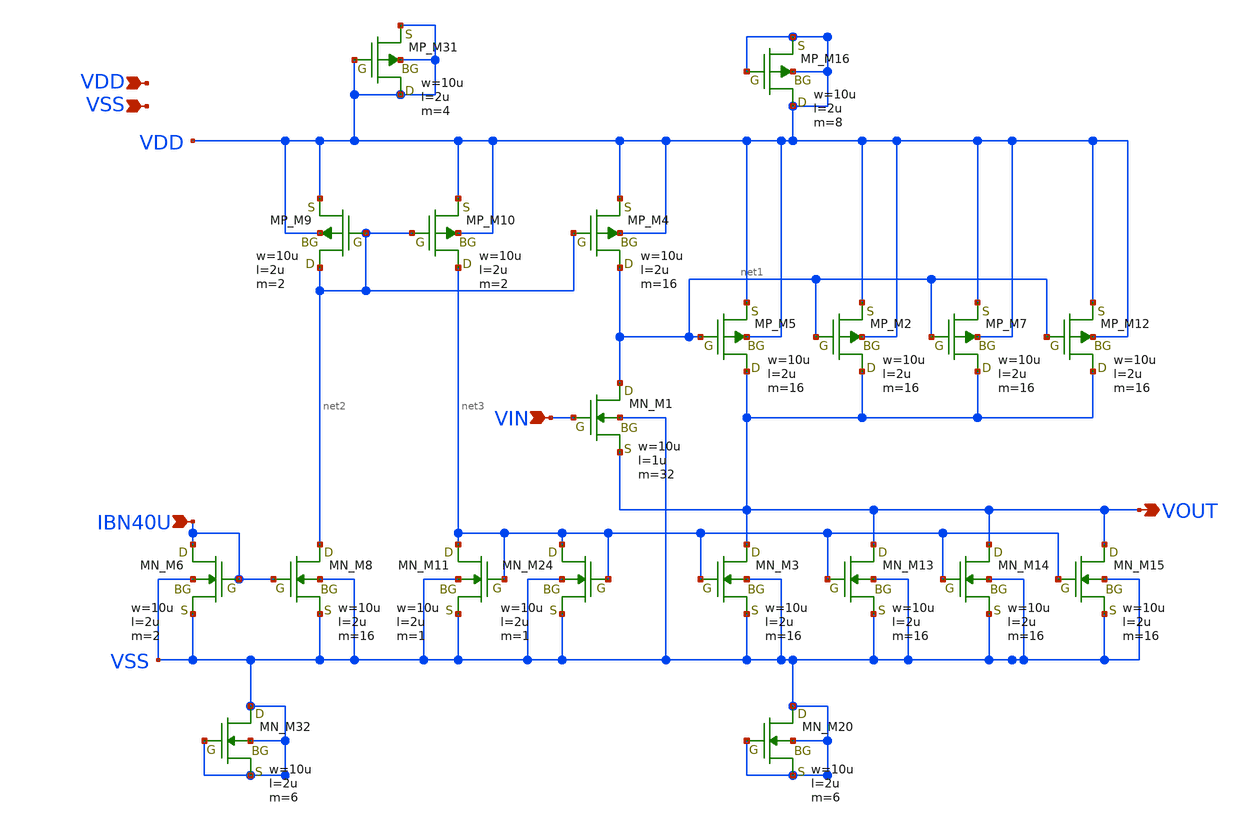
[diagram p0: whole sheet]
** sch_path: member_project/JJY_Receiver/Masahiro/jjy_recv/OBUF_SSF/BUF_SSF.sch
**.subckt BUF_SSF VDD VSS VIN IBN40U VOUT
*.ipin VDD
*.ipin VSS
*.ipin VIN
*.ipin IBN40U
*.opin VOUT
XM1 net1 VIN VOUT VSS NMOS w=10u l=1u as=0 ad=0 ps=0 pd=0 nrd=0 nrs=0 m=32
XM3 VOUT net3 VSS VSS NMOS w=10u l=2u as=0 ad=0 ps=0 pd=0 nrd=0 nrs=0 m=16
XM6 IBN40U IBN40U VSS VSS NMOS w=10u l=2u as=0 ad=0 ps=0 pd=0 nrd=0 nrs=0 m=2
XM4 net1 net2 VDD VDD PMOS w=10u l=2u as=0 ad=0 ps=0 pd=0 nrd=0 nrs=0 m=16
XM5 VOUT net1 VDD VDD PMOS w=10u l=2u as=0 ad=0 ps=0 pd=0 nrd=0 nrs=0 m=16
XM8 net2 IBN40U VSS VSS NMOS w=10u l=2u as=0 ad=0 ps=0 pd=0 nrd=0 nrs=0 m=16
XM9 net2 net2 VDD VDD PMOS w=10u l=2u as=0 ad=0 ps=0 pd=0 nrd=0 nrs=0 m=2
XM10 net3 net2 VDD VDD PMOS w=10u l=2u as=0 ad=0 ps=0 pd=0 nrd=0 nrs=0 m=2
XM11 net3 net3 VSS VSS NMOS w=10u l=2u as=0 ad=0 ps=0 pd=0 nrd=0 nrs=0 m=1
XM2 VOUT net1 VDD VDD PMOS w=10u l=2u as=0 ad=0 ps=0 pd=0 nrd=0 nrs=0 m=16
XM7 VOUT net1 VDD VDD PMOS w=10u l=2u as=0 ad=0 ps=0 pd=0 nrd=0 nrs=0 m=16
XM12 VOUT net1 VDD VDD PMOS w=10u l=2u as=0 ad=0 ps=0 pd=0 nrd=0 nrs=0 m=16
XM13 VOUT net3 VSS VSS NMOS w=10u l=2u as=0 ad=0 ps=0 pd=0 nrd=0 nrs=0 m=16
XM14 VOUT net3 VSS VSS NMOS w=10u l=2u as=0 ad=0 ps=0 pd=0 nrd=0 nrs=0 m=16
XM15 VOUT net3 VSS VSS NMOS w=10u l=2u as=0 ad=0 ps=0 pd=0 nrd=0 nrs=0 m=16
XM16 VDD VDD VDD VDD PMOS w=10u l=2u as=0 ad=0 ps=0 pd=0 nrd=0 nrs=0 m=8
XM24 net3 net3 VSS VSS NMOS w=10u l=2u as=0 ad=0 ps=0 pd=0 nrd=0 nrs=0 m=1
XM20 VSS VSS VSS VSS NMOS w=10u l=2u as=0 ad=0 ps=0 pd=0 nrd=0 nrs=0 m=6
XM31 VDD VDD VDD VDD PMOS w=10u l=2u as=0 ad=0 ps=0 pd=0 nrd=0 nrs=0 m=4
XM32 VSS VSS VSS VSS NMOS w=10u l=2u as=0 ad=0 ps=0 pd=0 nrd=0 nrs=0 m=6
**.ends
.end
